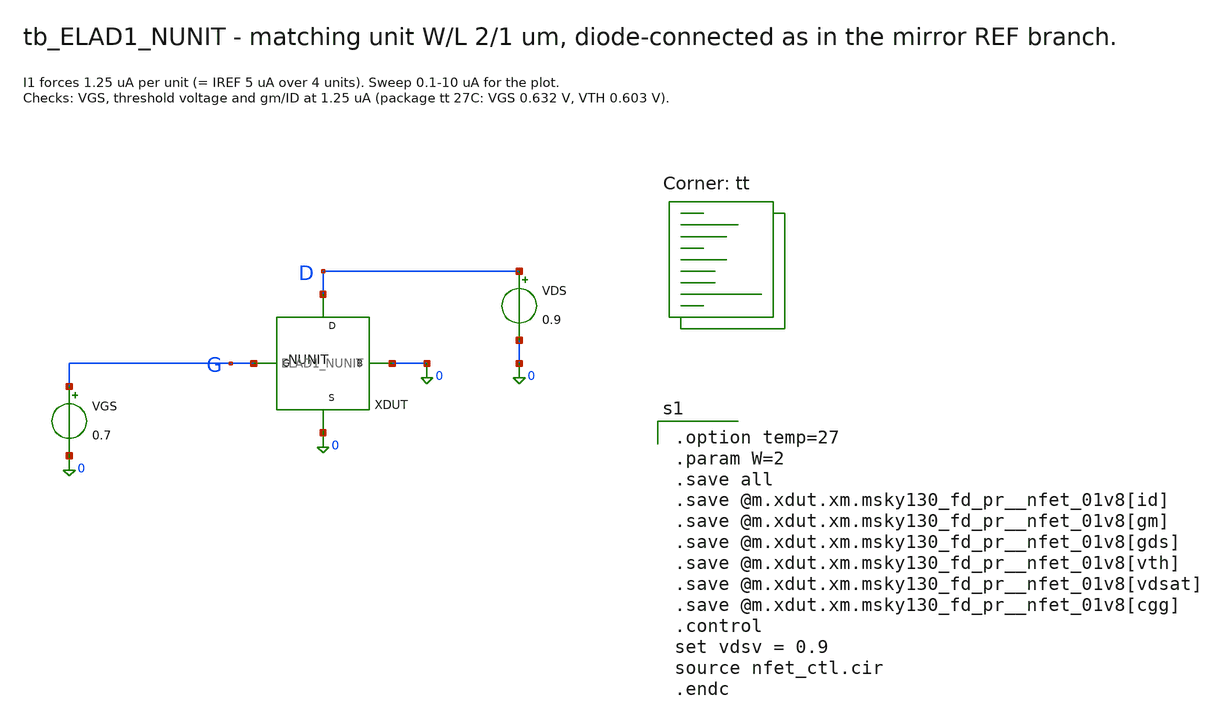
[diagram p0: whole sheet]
** sch_path: cells/ELAD1_NUNIT/schematic/tb_ELAD1_NUNIT.sch
**.subckt tb_ELAD1_NUNIT
XDUT D G 0 0 ELAD1_NUNIT
VGS G 0 0.7
VDS D 0 0.9
**** begin user architecture code

.option temp=27
.param W=2
.save all
.save @m.xdut.xm.msky130_fd_pr__nfet_01v8[id]
.save @m.xdut.xm.msky130_fd_pr__nfet_01v8[gm]
.save @m.xdut.xm.msky130_fd_pr__nfet_01v8[gds]
.save @m.xdut.xm.msky130_fd_pr__nfet_01v8[vth]
.save @m.xdut.xm.msky130_fd_pr__nfet_01v8[vdsat]
.save @m.xdut.xm.msky130_fd_pr__nfet_01v8[cgg]
.control
set vdsv = 0.9
source nfet_ctl.cir
.endc

.lib $::SKYWATER_MODELS/sky130.lib.spice tt
**** end user architecture code
**.ends

* expanding   symbol:  ELAD1_NUNIT.sym # of pins=4
** sym_path: cells/ELAD1_NUNIT/schematic/ELAD1_NUNIT.sym
** sch_path: cells/ELAD1_NUNIT/schematic/ELAD1_NUNIT.sch
.subckt ELAD1_NUNIT D G S B
*.iopin D
*.iopin G
*.iopin S
*.iopin B
XM D G S B sky130_fd_pr__nfet_01v8 L=1 W={W} nf=1 ad='int((1 + 1)/2) * {W} / 1 * 0.29' as='int((1 + 2)/2) * {W} / 1 * 0.29'
+ pd='2*int((1 + 1)/2) * ({W} / 1 + 0.29)' ps='2*int((1 + 2)/2) * ({W} / 1 + 0.29)' nrd='0.29 / {W} ' nrs='0.29 / {W} '
+ sa=0 sb=0 sd=0 mult=1 m=1
.ends

.end
